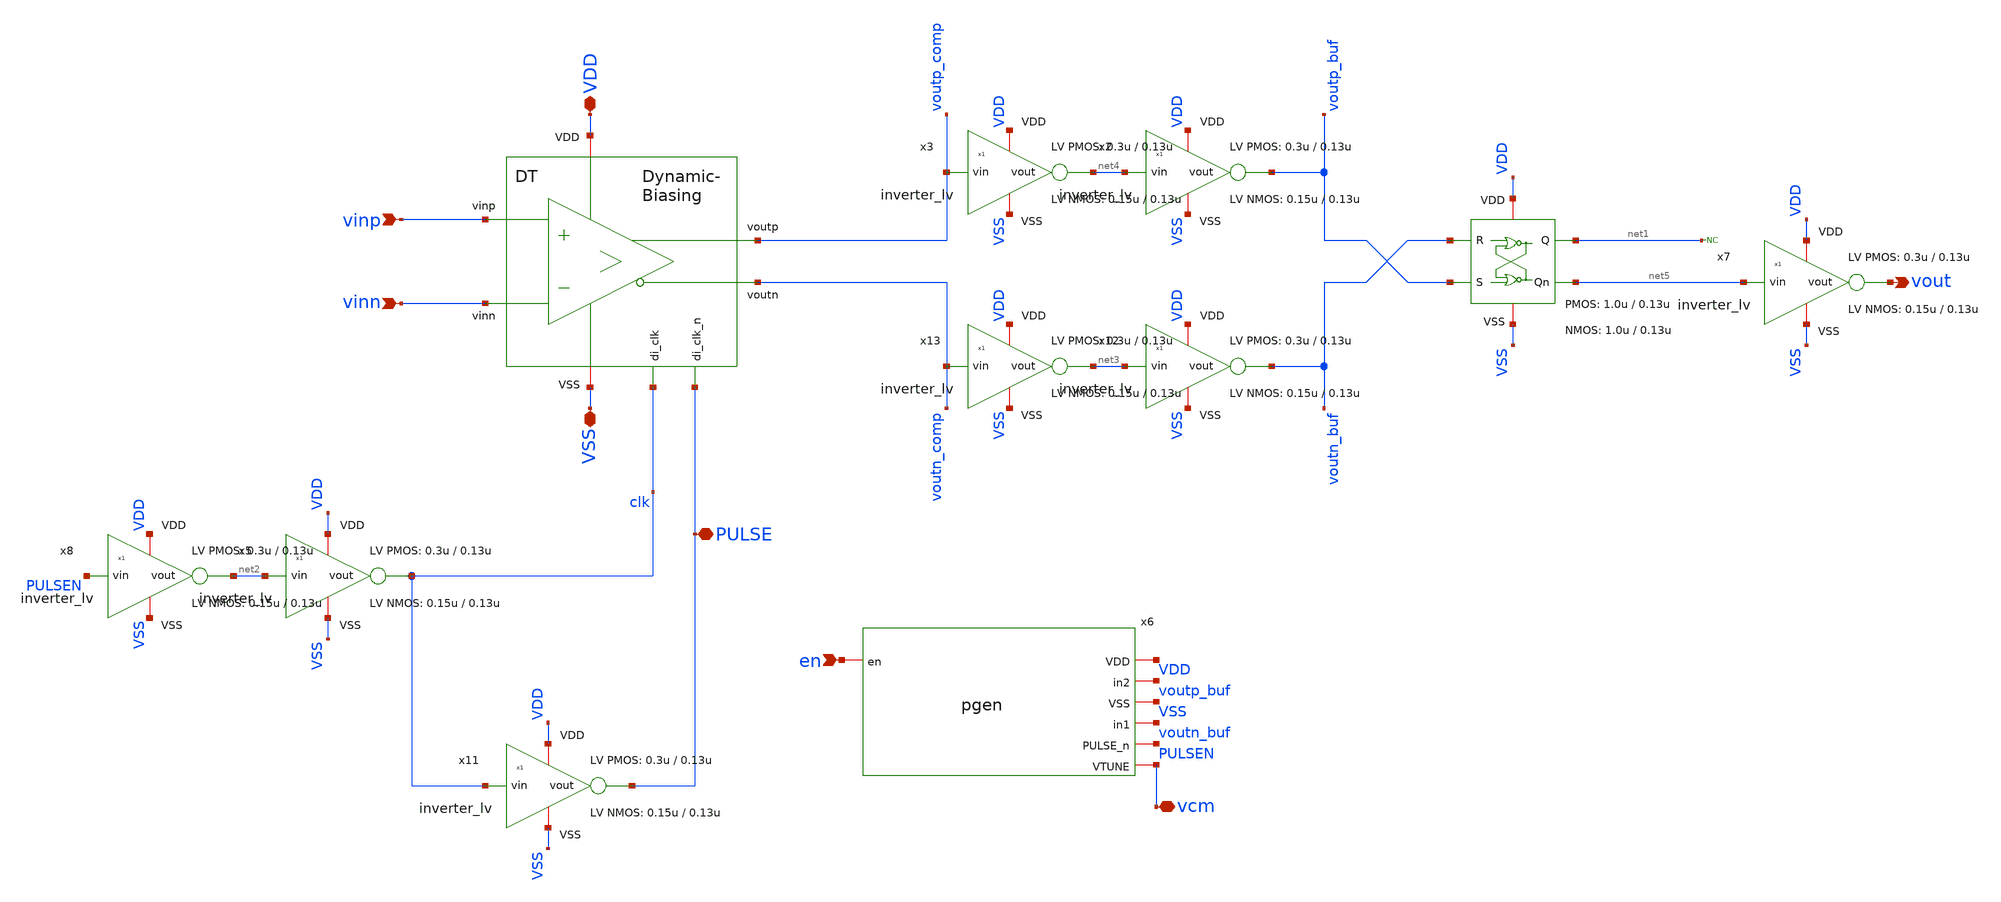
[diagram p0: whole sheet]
** sch_path: xschem/comparator/discrete_time/DT_comparator.sch
**.subckt DT_comparator VDD vout VSS vinp vinn en PULSE vcm
*.iopin VDD
*.opin vout
*.iopin VSS
*.ipin vinp
*.ipin vinn
*.ipin en
*.iopin PULSE
*.iopin vcm
x5 VDD net2 clk VSS inverter_lv W_P=0.3u L_P=0.13u W_N=0.15u L_N=0.13u N_C=1
* noconn #net1
x4 VDD voutp_buf net5 VSS net1 voutn_buf SR_latch W_P_SR=1.0u L_P_SR=0.13u W_N_SR=1.0u L_N_SR=0.13u
x6 VDD voutp_buf VSS voutn_buf PULSEN vcm en pgen
x1 PULSE clk VDD voutp_comp vinp VSS voutn_comp vinn dynamic_biasing_comparator
x8 VDD PULSEN net2 VSS inverter_lv W_P=0.3u L_P=0.13u W_N=0.15u L_N=0.13u N_C=1
x11 VDD clk PULSE VSS inverter_lv W_P=0.3u L_P=0.13u W_N=0.15u L_N=0.13u N_C=1
x12 VDD net3 voutn_buf VSS inverter_lv W_P=0.3u L_P=0.13u W_N=0.15u L_N=0.13u N_C=1
x13 VDD voutn_comp net3 VSS inverter_lv W_P=0.3u L_P=0.13u W_N=0.15u L_N=0.13u N_C=1
x2 VDD net4 voutp_buf VSS inverter_lv W_P=0.3u L_P=0.13u W_N=0.15u L_N=0.13u N_C=1
x3 VDD voutp_comp net4 VSS inverter_lv W_P=0.3u L_P=0.13u W_N=0.15u L_N=0.13u N_C=1
x7 VDD net5 vout VSS inverter_lv W_P=0.3u L_P=0.13u W_N=0.15u L_N=0.13u N_C=1
**.ends
.end
